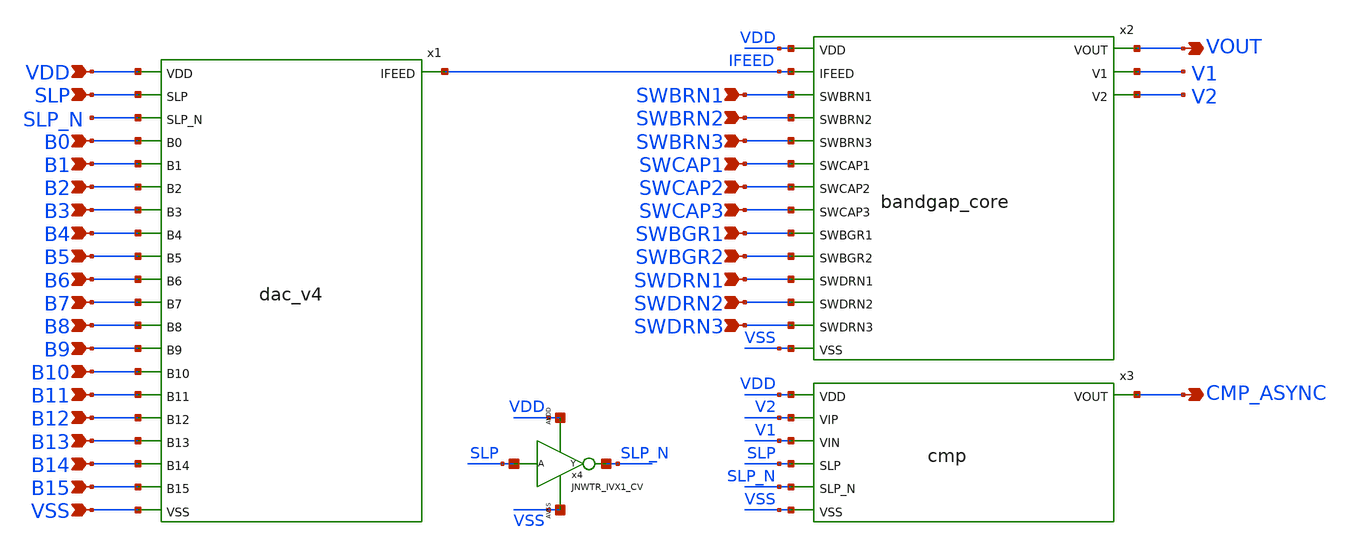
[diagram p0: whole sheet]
** sch_path: design/LELO_TORD_SKY130A/TB_reference.sch
**.subckt TB_reference B1 B2 B3 B4 VSS VDD SLP B0 B5 B6 B7 SWDRN1 SWBRN1 SWBRN2 SWCAP1 SWCAP2 SWBGR1
*+ SWBGR2 SWDRN2 SWDRN3 SWCAP3 SWBRN3 B8 B9 B10 B11 B12 B13 B14 B15 VOUT CMP_ASYNC
*.ipin B1
*.ipin B2
*.ipin B3
*.ipin B4
*.ipin VSS
*.ipin VDD
*.ipin SLP
*.ipin B0
*.ipin B5
*.ipin B6
*.ipin B7
*.ipin SWDRN1
*.ipin SWBRN1
*.ipin SWBRN2
*.ipin SWCAP1
*.ipin SWCAP2
*.ipin SWBGR1
*.ipin SWBGR2
*.ipin SWDRN2
*.ipin SWDRN3
*.ipin SWCAP3
*.ipin SWBRN3
*.ipin B8
*.ipin B9
*.ipin B10
*.ipin B11
*.ipin B12
*.ipin B13
*.ipin B14
*.ipin B15
*.opin VOUT
*.opin CMP_ASYNC
x1 VDD SLP SLP_N B0 B1 B2 B3 B4 B5 B6 B7 B8 B9 B10 B11 IFEED B12 B13 B14 B15 VSS dac_v4
x3 VDD CMP_ASYNC V2 V1 SLP SLP_N VSS cmp
x4 SLP SLP_N VDD VSS JNWTR_IVX1_CV
x2 VDD IFEED SWBRN1 SWBRN2 SWBRN3 SWCAP1 SWCAP2 VOUT V1 SWCAP3 SWBGR1 V2 SWBGR2 SWDRN1 SWDRN2 SWDRN3
+ VSS bandgap_core
**.ends
.end
